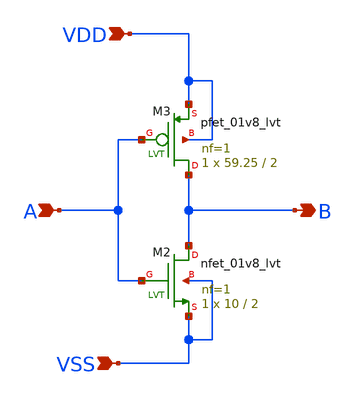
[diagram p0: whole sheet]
** sch_path: inverseur.sch
**.subckt inverseur VDD VSS A B
*.ipin VDD
*.ipin VSS
*.ipin A
*.opin B
XM2 B A VSS VSS sky130_fd_pr__nfet_01v8_lvt L=2 W=10 nf=1 ad='int((nf+1)/2) * W/nf * 0.29' as='int((nf+2)/2) * W/nf * 0.29'
+ pd='2*int((nf+1)/2) * (W/nf + 0.29)' ps='2*int((nf+2)/2) * (W/nf + 0.29)' nrd='0.29 / W' nrs='0.29 / W'
+ sa=0 sb=0 sd=0 mult=1 m=1
XM3 B A VDD VDD sky130_fd_pr__pfet_01v8_lvt L=2 W=59.25 nf=1 ad='int((nf+1)/2) * W/nf * 0.29' as='int((nf+2)/2) * W/nf * 0.29'
+ pd='2*int((nf+1)/2) * (W/nf + 0.29)' ps='2*int((nf+2)/2) * (W/nf + 0.29)' nrd='0.29 / W' nrs='0.29 / W'
+ sa=0 sb=0 sd=0 mult=1 m=1
**.ends
.end
